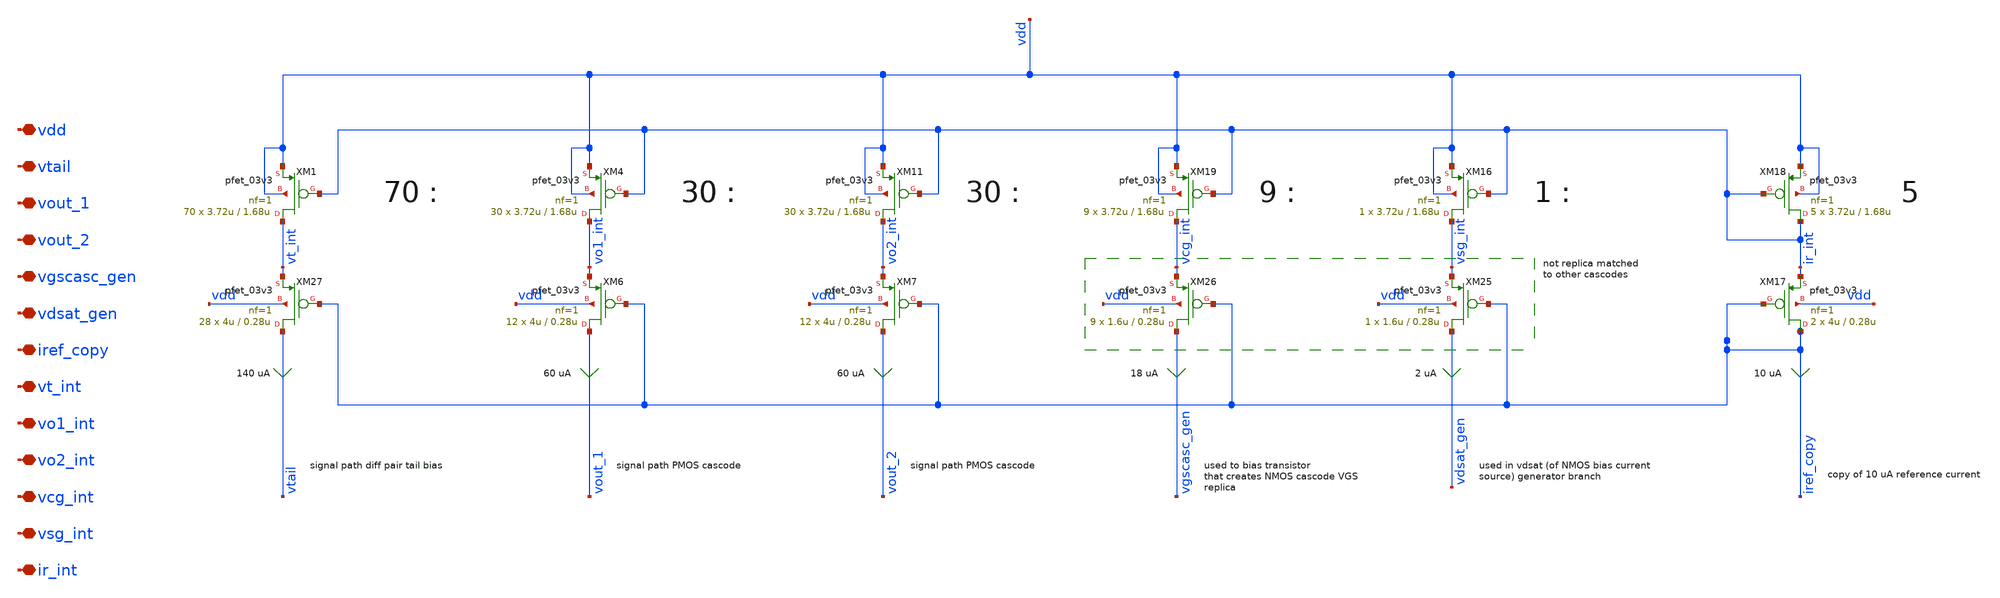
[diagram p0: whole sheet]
** sch_path: xschem/ccia_main_ota/b9_ccia_main_ota_s1_pmos_bias.sch
**.subckt b9_ccia_main_ota_s1_pmos_bias vdd vtail vout_1 vout_2 vgscasc_gen vdsat_gen iref_copy
*+ vt_int vo1_int vo2_int vcg_int vsg_int ir_int
*.iopin vdd
*.iopin vtail
*.iopin vout_1
*.iopin vout_2
*.iopin vgscasc_gen
*.iopin vdsat_gen
*.iopin iref_copy
*.iopin vt_int
*.iopin vo1_int
*.iopin vo2_int
*.iopin vcg_int
*.iopin vsg_int
*.iopin ir_int
XM1 vt_int ir_int vdd vdd pfet_03v3 L=1.68u W=3.72u nf=1 ad='int((nf+1)/2) * W/nf * 0.18u' as='int((nf+2)/2) * W/nf * 0.18u'
+ pd='2*int((nf+1)/2) * (W/nf + 0.18u)' ps='2*int((nf+2)/2) * (W/nf + 0.18u)' nrd='0.18u / W' nrs='0.18u / W'
+ sa=0 sb=0 sd=0 m=70
XM7 vout_2 iref_copy vo2_int vdd pfet_03v3 L=0.28u W=4u nf=1 ad='int((nf+1)/2) * W/nf * 0.18u' as='int((nf+2)/2) * W/nf * 0.18u'
+ pd='2*int((nf+1)/2) * (W/nf + 0.18u)' ps='2*int((nf+2)/2) * (W/nf + 0.18u)' nrd='0.18u / W' nrs='0.18u / W'
+ sa=0 sb=0 sd=0 m=12
XM17 iref_copy iref_copy ir_int vdd pfet_03v3 L=0.28u W=4u nf=1 ad='int((nf+1)/2) * W/nf * 0.18u' as='int((nf+2)/2) * W/nf * 0.18u'
+ pd='2*int((nf+1)/2) * (W/nf + 0.18u)' ps='2*int((nf+2)/2) * (W/nf + 0.18u)' nrd='0.18u / W' nrs='0.18u / W'
+ sa=0 sb=0 sd=0 m=2
XM18 ir_int ir_int vdd vdd pfet_03v3 L=1.68u W=3.72u nf=1 ad='int((nf+1)/2) * W/nf * 0.18u' as='int((nf+2)/2) * W/nf * 0.18u'
+ pd='2*int((nf+1)/2) * (W/nf + 0.18u)' ps='2*int((nf+2)/2) * (W/nf + 0.18u)' nrd='0.18u / W' nrs='0.18u / W'
+ sa=0 sb=0 sd=0 m=5
XM4 vo1_int ir_int vdd vdd pfet_03v3 L=1.68u W=3.72u nf=1 ad='int((nf+1)/2) * W/nf * 0.18u' as='int((nf+2)/2) * W/nf * 0.18u'
+ pd='2*int((nf+1)/2) * (W/nf + 0.18u)' ps='2*int((nf+2)/2) * (W/nf + 0.18u)' nrd='0.18u / W' nrs='0.18u / W'
+ sa=0 sb=0 sd=0 m=30
XM16 vsg_int ir_int vdd vdd pfet_03v3 L=1.68u W=3.72u nf=1 ad='int((nf+1)/2) * W/nf * 0.18u' as='int((nf+2)/2) * W/nf * 0.18u'
+ pd='2*int((nf+1)/2) * (W/nf + 0.18u)' ps='2*int((nf+2)/2) * (W/nf + 0.18u)' nrd='0.18u / W' nrs='0.18u / W'
+ sa=0 sb=0 sd=0 m=1
XM19 vcg_int ir_int vdd vdd pfet_03v3 L=1.68u W=3.72u nf=1 ad='int((nf+1)/2) * W/nf * 0.18u' as='int((nf+2)/2) * W/nf * 0.18u'
+ pd='2*int((nf+1)/2) * (W/nf + 0.18u)' ps='2*int((nf+2)/2) * (W/nf + 0.18u)' nrd='0.18u / W' nrs='0.18u / W'
+ sa=0 sb=0 sd=0 m=9
XM11 vo2_int ir_int vdd vdd pfet_03v3 L=1.68u W=3.72u nf=1 ad='int((nf+1)/2) * W/nf * 0.18u' as='int((nf+2)/2) * W/nf * 0.18u'
+ pd='2*int((nf+1)/2) * (W/nf + 0.18u)' ps='2*int((nf+2)/2) * (W/nf + 0.18u)' nrd='0.18u / W' nrs='0.18u / W'
+ sa=0 sb=0 sd=0 m=30
XM6 vout_1 iref_copy vo1_int vdd pfet_03v3 L=0.28u W=4u nf=1 ad='int((nf+1)/2) * W/nf * 0.18u' as='int((nf+2)/2) * W/nf * 0.18u'
+ pd='2*int((nf+1)/2) * (W/nf + 0.18u)' ps='2*int((nf+2)/2) * (W/nf + 0.18u)' nrd='0.18u / W' nrs='0.18u / W'
+ sa=0 sb=0 sd=0 m=12
XM25 vdsat_gen iref_copy vsg_int vdd pfet_03v3 L=0.28u W=1.6u nf=1 ad='int((nf+1)/2) * W/nf * 0.18u'
+ as='int((nf+2)/2) * W/nf * 0.18u' pd='2*int((nf+1)/2) * (W/nf + 0.18u)' ps='2*int((nf+2)/2) * (W/nf + 0.18u)'
+ nrd='0.18u / W' nrs='0.18u / W' sa=0 sb=0 sd=0 m=1
XM26 vgscasc_gen iref_copy vcg_int vdd pfet_03v3 L=0.28u W=1.6u nf=1 ad='int((nf+1)/2) * W/nf * 0.18u'
+ as='int((nf+2)/2) * W/nf * 0.18u' pd='2*int((nf+1)/2) * (W/nf + 0.18u)' ps='2*int((nf+2)/2) * (W/nf + 0.18u)'
+ nrd='0.18u / W' nrs='0.18u / W' sa=0 sb=0 sd=0 m=9
XM27 vtail iref_copy vt_int vdd pfet_03v3 L=0.28u W=4u nf=1 ad='int((nf+1)/2) * W/nf * 0.18u' as='int((nf+2)/2) * W/nf * 0.18u'
+ pd='2*int((nf+1)/2) * (W/nf + 0.18u)' ps='2*int((nf+2)/2) * (W/nf + 0.18u)' nrd='0.18u / W' nrs='0.18u / W'
+ sa=0 sb=0 sd=0 m=28
**.ends
.end
